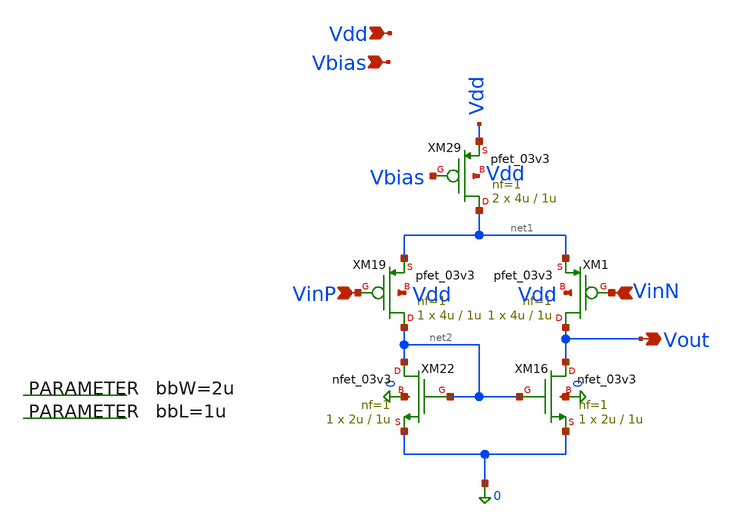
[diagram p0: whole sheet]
** sch_path: blocks/dac/common/ota5t.sch
**.subckt ota5t VinP VinN Vout Vdd Vbias
*.ipin VinP
*.ipin VinN
*.opin Vout
*.ipin Vdd
*.ipin Vbias
XM16 Vout net2 0 0 nfet_03v3 L=1u W=2u nf=1 ad='int((nf+1)/2) * W/nf * 0.18u' as='int((nf+2)/2) * W/nf * 0.18u'
+ pd='2*int((nf+1)/2) * (W/nf + 0.18u)' ps='2*int((nf+2)/2) * (W/nf + 0.18u)' nrd='0.18u / W' nrs='0.18u / W'
+ sa=0 sb=0 sd=0 m=1
XM1 Vout VinN net1 Vdd pfet_03v3 L=1u W=4u nf=1 ad='int((nf+1)/2) * W/nf * 0.18u' as='int((nf+2)/2) * W/nf * 0.18u'
+ pd='2*int((nf+1)/2) * (W/nf + 0.18u)' ps='2*int((nf+2)/2) * (W/nf + 0.18u)' nrd='0.18u / W' nrs='0.18u / W'
+ sa=0 sb=0 sd=0 m=1
XM19 net2 VinP net1 Vdd pfet_03v3 L=1u W=4u nf=1 ad='int((nf+1)/2) * W/nf * 0.18u' as='int((nf+2)/2) * W/nf * 0.18u'
+ pd='2*int((nf+1)/2) * (W/nf + 0.18u)' ps='2*int((nf+2)/2) * (W/nf + 0.18u)' nrd='0.18u / W' nrs='0.18u / W'
+ sa=0 sb=0 sd=0 m=1
XM22 net2 net2 0 0 nfet_03v3 L=1u W=2u nf=1 ad='int((nf+1)/2) * W/nf * 0.18u' as='int((nf+2)/2) * W/nf * 0.18u'
+ pd='2*int((nf+1)/2) * (W/nf + 0.18u)' ps='2*int((nf+2)/2) * (W/nf + 0.18u)' nrd='0.18u / W' nrs='0.18u / W'
+ sa=0 sb=0 sd=0 m=1
.param bbW=2u
.param bbL=1u
XM29 net1 Vbias Vdd Vdd pfet_03v3 L=1u W=4u nf=1 ad='int((nf+1)/2) * W/nf * 0.18u' as='int((nf+2)/2) * W/nf * 0.18u'
+ pd='2*int((nf+1)/2) * (W/nf + 0.18u)' ps='2*int((nf+2)/2) * (W/nf + 0.18u)' nrd='0.18u / W' nrs='0.18u / W'
+ sa=0 sb=0 sd=0 m=2
**.ends
.end
